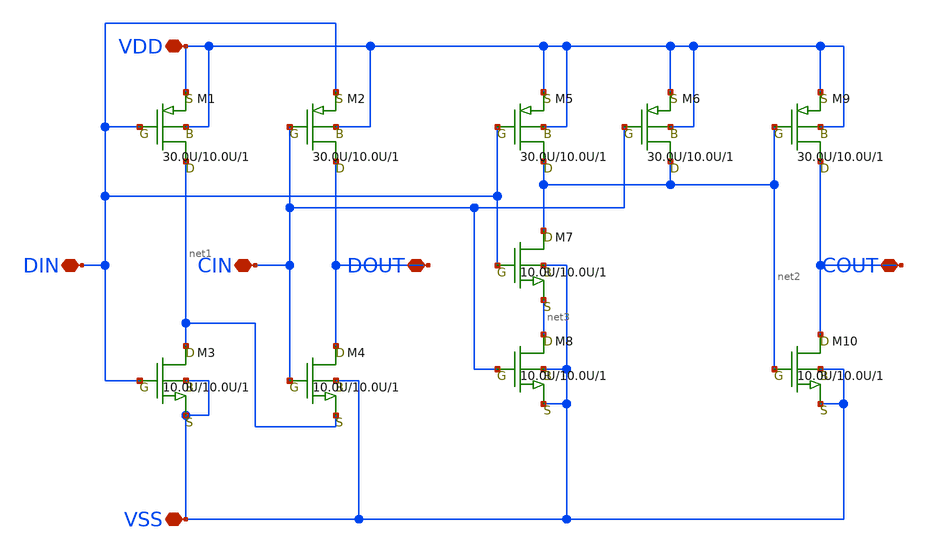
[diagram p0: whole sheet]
** sch_path: xschem/counter_stage_min.sch
**.subckt counter_stage_min VDD VSS DIN CIN DOUT COUT
*.iopin VDD
*.iopin VSS
*.iopin DIN
*.iopin CIN
*.iopin DOUT
*.iopin COUT
M1 net1 DIN VDD VDD pch w=30.0U l=10.0U as=0 ps=0 ad=0 pd=0 m=1
M3 net1 DIN VSS VSS nch w=10.0U l=10.0U as=0 ps=0 ad=0 pd=0 m=1
M2 DOUT CIN DIN VDD pch w=30.0U l=10.0U as=0 ps=0 ad=0 pd=0 m=1
M4 DOUT CIN net1 VSS nch w=10.0U l=10.0U as=0 ps=0 ad=0 pd=0 m=1
M5 net2 DIN VDD VDD pch w=30.0U l=10.0U as=0 ps=0 ad=0 pd=0 m=1
M6 net2 CIN VDD VDD pch w=30.0U l=10.0U as=0 ps=0 ad=0 pd=0 m=1
M7 net2 DIN net3 VSS nch w=10.0U l=10.0U as=0 ps=0 ad=0 pd=0 m=1
M8 net3 CIN VSS VSS nch w=10.0U l=10.0U as=0 ps=0 ad=0 pd=0 m=1
M9 COUT net2 VDD VDD pch w=30.0U l=10.0U as=0 ps=0 ad=0 pd=0 m=1
M10 COUT net2 VSS VSS nch w=10.0U l=10.0U as=0 ps=0 ad=0 pd=0 m=1
**.ends
.end
